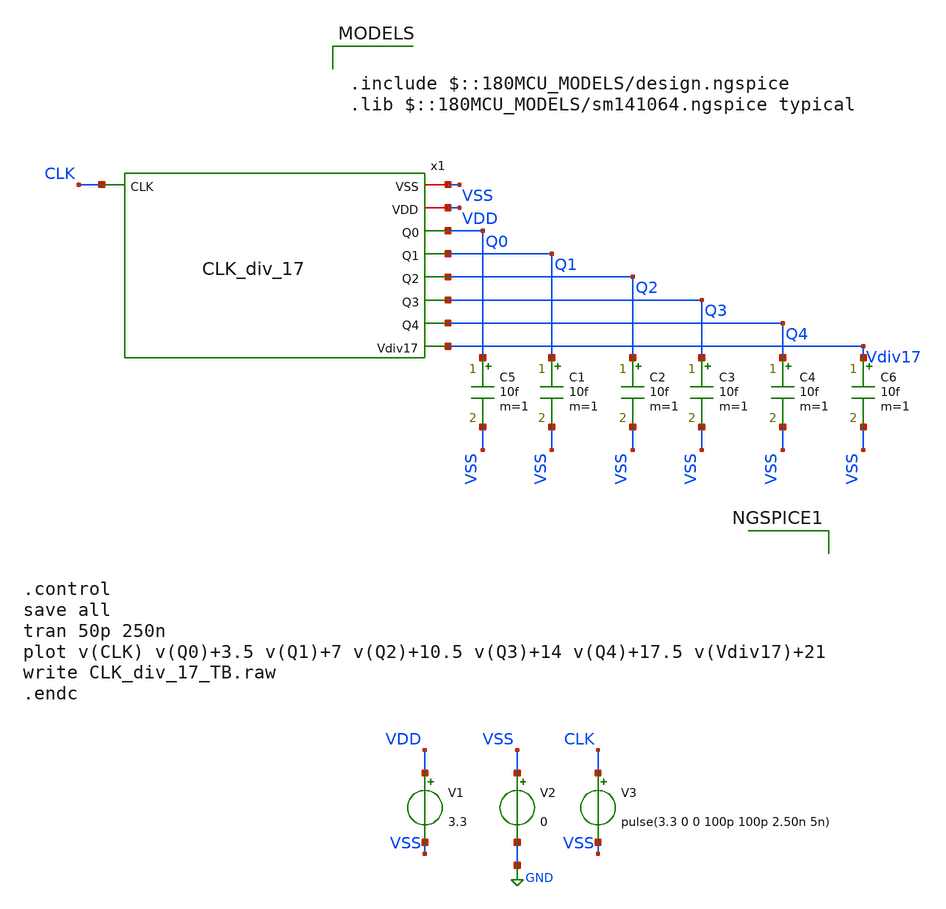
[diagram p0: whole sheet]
** sch_path: Clock_Generator_PAKISTAN_02/Schematics/CLK_div_17_TB.sch
**.subckt CLK_div_17_TB
V1 VDD VSS 3.3
V2 VSS GND 0
V3 CLK VSS pulse(3.3 0 0 100p 100p 2.50n 5n)
C5 Q0 VSS 10f m=1
C1 Q1 VSS 10f m=1
C2 Q2 VSS 10f m=1
C3 Q3 VSS 10f m=1
C4 Q4 VSS 10f m=1
C6 Vdiv17 VSS 10f m=1
x1 VSS VDD Q0 Q1 Q2 Q3 Q4 Vdiv17 CLK CLK_div_17
**** begin user architecture code

.include $::180MCU_MODELS/design.ngspice
.lib $::180MCU_MODELS/sm141064.ngspice typical




.control
save all
tran 50p 250n
plot v(CLK) v(Q0)+3.5 v(Q1)+7 v(Q2)+10.5 v(Q3)+14 v(Q4)+17.5 v(Vdiv17)+21
write CLK_div_17_TB.raw
.endc


**** end user architecture code
**.ends
.GLOBAL GND
.end
